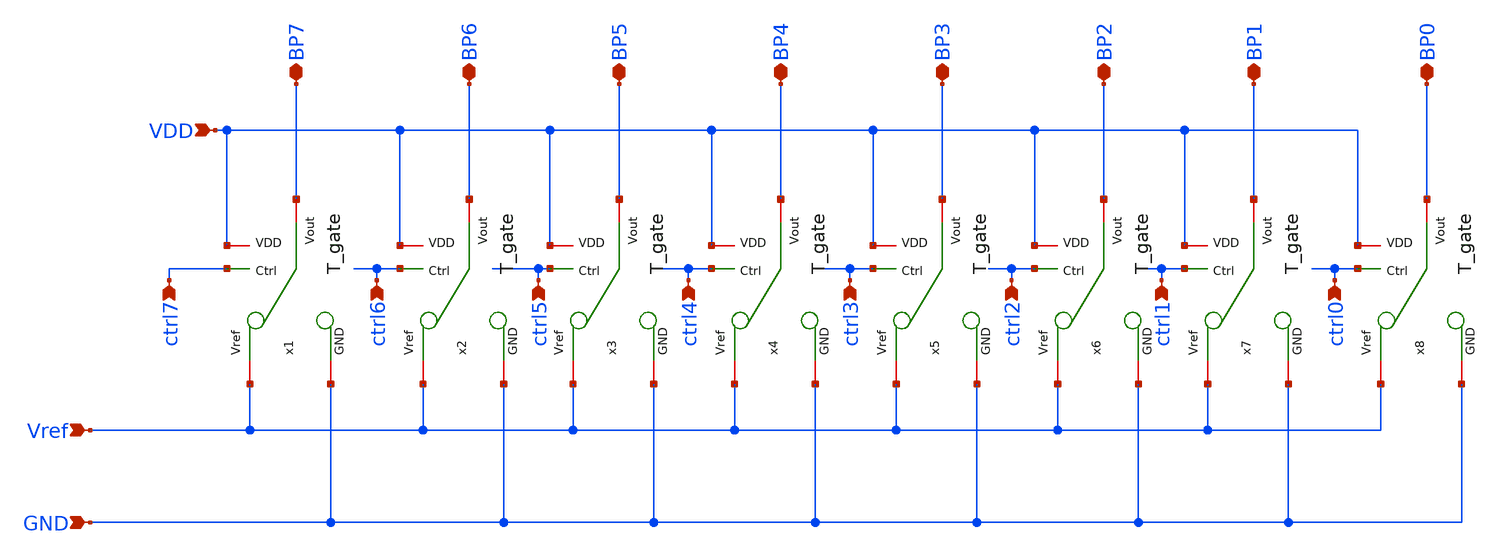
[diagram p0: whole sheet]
** sch_path: 05_mixed_signal/soluzioni/lab03/xschem/switch_bank.sch
**.subckt switch_bank Vref GND BP7 BP6 BP5 BP4 BP3 BP2 BP1 BP0 VDD ctrl7 ctrl6 ctrl5 ctrl4 ctrl3
*+ ctrl2 ctrl1 ctrl0
*.ipin Vref
*.ipin GND
*.iopin BP7
*.iopin BP6
*.iopin BP5
*.iopin BP4
*.iopin BP3
*.iopin BP2
*.iopin BP1
*.iopin BP0
*.ipin VDD
*.ipin ctrl7
*.ipin ctrl6
*.ipin ctrl5
*.ipin ctrl4
*.ipin ctrl3
*.ipin ctrl2
*.ipin ctrl1
*.ipin ctrl0
x1 VDD GND ctrl7 BP7 Vref T_gate
x2 VDD GND ctrl6 BP6 Vref T_gate
x3 VDD GND ctrl5 BP5 Vref T_gate
x4 VDD GND ctrl4 BP4 Vref T_gate
x5 VDD GND ctrl3 BP3 Vref T_gate
x6 VDD GND ctrl2 BP2 Vref T_gate
x7 VDD GND ctrl1 BP1 Vref T_gate
x8 VDD GND ctrl0 BP0 Vref T_gate
**.ends

* expanding   symbol:  T_gate.sym # of pins=5
** sym_path: 05_mixed_signal/soluzioni/lab01/xschem/T_gate.sym
** sch_path: 05_mixed_signal/soluzioni/lab01/xschem/T_gate.sch
.subckt T_gate VDD GND Ctrl Vout Vref
*.ipin Ctrl
*.iopin Vout
*.iopin VDD
*.iopin GND
*.iopin Vref
x1 VDD Ctrl net1 GND inverter
XM1 GND net1 Vout GND sky130_fd_pr__nfet_01v8_lvt L=0.15 W=2 nf=1 ad='int((1 + 1)/2) * 2 / 1 * 0.29'
+ as='int((1 + 2)/2) * 2 / 1 * 0.29' pd='2*int((1 + 1)/2) * (2 / 1 + 0.29)' ps='2*int((1 + 2)/2) * (2 / 1 + 0.29)'
+ nrd='0.29 / 2 ' nrs='0.29 / 2 ' sa=0 sb=0 sd=0 mult=1 m=1
XM2 GND Ctrl Vout VDD sky130_fd_pr__pfet_01v8_lvt L=0.35 W=4 nf=1 ad='int((1 + 1)/2) * 4 / 1 * 0.29'
+ as='int((1 + 2)/2) * 4 / 1 * 0.29' pd='2*int((1 + 1)/2) * (4 / 1 + 0.29)' ps='2*int((1 + 2)/2) * (4 / 1 + 0.29)'
+ nrd='0.29 / 4 ' nrs='0.29 / 4 ' sa=0 sb=0 sd=0 mult=1 m=1
XM3 Vref Ctrl Vout GND sky130_fd_pr__nfet_01v8_lvt L=0.15 W=2 nf=1 ad='int((1 + 1)/2) * 2 / 1 * 0.29'
+ as='int((1 + 2)/2) * 2 / 1 * 0.29' pd='2*int((1 + 1)/2) * (2 / 1 + 0.29)' ps='2*int((1 + 2)/2) * (2 / 1 + 0.29)'
+ nrd='0.29 / 2 ' nrs='0.29 / 2 ' sa=0 sb=0 sd=0 mult=1 m=1
XM4 Vref net1 Vout VDD sky130_fd_pr__pfet_01v8_lvt L=0.35 W=4 nf=1 ad='int((1 + 1)/2) * 4 / 1 * 0.29'
+ as='int((1 + 2)/2) * 4 / 1 * 0.29' pd='2*int((1 + 1)/2) * (4 / 1 + 0.29)' ps='2*int((1 + 2)/2) * (4 / 1 + 0.29)'
+ nrd='0.29 / 4 ' nrs='0.29 / 4 ' sa=0 sb=0 sd=0 mult=1 m=1
.ends


* expanding   symbol:  inverter.sym # of pins=4
** sym_path: 05_mixed_signal/soluzioni/lab03/xschem/inverter.sym
** sch_path: 05_mixed_signal/soluzioni/lab03/xschem/inverter.sch
.subckt inverter VDD IN OUT GND
*.ipin IN
*.opin OUT
*.iopin VDD
*.iopin GND
XM1 OUT IN GND GND sky130_fd_pr__nfet_01v8_lvt L=0.15 W=2 nf=1 ad='int((1 + 1)/2) * 2 / 1 * 0.29' as='int((1 + 2)/2) * 2 / 1 * 0.29'
+ pd='2*int((1 + 1)/2) * (2 / 1 + 0.29)' ps='2*int((1 + 2)/2) * (2 / 1 + 0.29)' nrd='0.29 / 2 ' nrs='0.29 / 2 '
+ sa=0 sb=0 sd=0 mult=1 m=1
XM2 OUT IN VDD VDD sky130_fd_pr__pfet_01v8_lvt L=0.35 W=4 nf=1 ad='int((1 + 1)/2) * 4 / 1 * 0.29' as='int((1 + 2)/2) * 4 / 1 * 0.29'
+ pd='2*int((1 + 1)/2) * (4 / 1 + 0.29)' ps='2*int((1 + 2)/2) * (4 / 1 + 0.29)' nrd='0.29 / 4 ' nrs='0.29 / 4 '
+ sa=0 sb=0 sd=0 mult=1 m=1
.ends

.end
